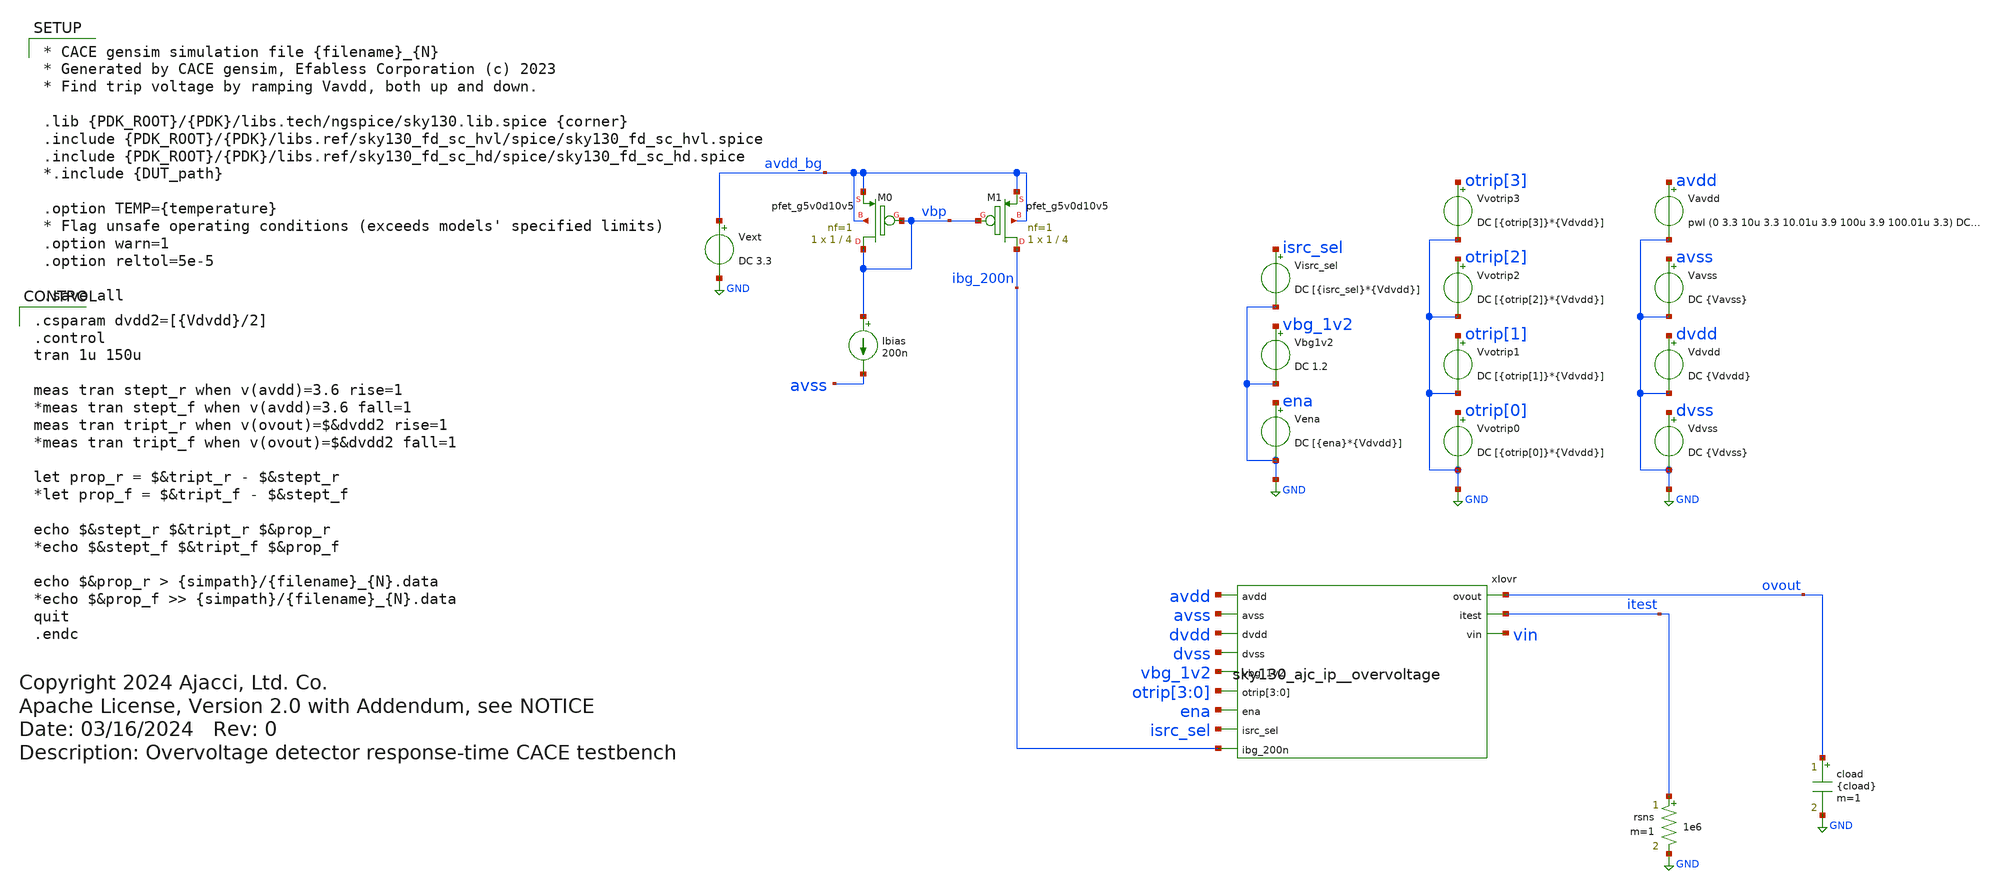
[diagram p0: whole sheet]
** sch_path: cace/response_time.sch
* Copyright 2024 Ajacci, Ltd. Co.
* Apache License, Version 2.0 with Addendum, see NOTICE
**.subckt response_time
Vavss avss GND DC {Vavss}
Vena ena GND DC [{ena}*{Vdvdd}]
Vavdd avdd GND pwl (0 3.3 10u 3.3 10.01u 3.9 100u 3.9 100.01u 3.3) DC {Vavdd}
.save i(vavdd)
Vbg1v2 vbg_1v2 GND DC 1.2
Ibias vbp avss 200n
XM1 ibg_200n vbp avdd_bg avdd_bg sky130_fd_pr__pfet_g5v0d10v5 L=4 W=1 nf=1 ad='int((nf+1)/2) * W/nf * 0.29'
+ as='int((nf+2)/2) * W/nf * 0.29' pd='2*int((nf+1)/2) * (W/nf + 0.29)' ps='2*int((nf+2)/2) * (W/nf + 0.29)'
+ nrd='0.29 / W' nrs='0.29 / W' sa=0 sb=0 sd=0 mult=1 m=1
XM0 vbp vbp avdd_bg avdd_bg sky130_fd_pr__pfet_g5v0d10v5 L=4 W=1 nf=1 ad='int((nf+1)/2) * W/nf * 0.29'
+ as='int((nf+2)/2) * W/nf * 0.29' pd='2*int((nf+1)/2) * (W/nf + 0.29)' ps='2*int((nf+2)/2) * (W/nf + 0.29)'
+ nrd='0.29 / W' nrs='0.29 / W' sa=0 sb=0 sd=0 mult=1 m=1
Vdvss dvss GND DC {Vdvss}
Vdvdd dvdd GND DC {Vdvdd}
.save i(vdvdd)
rsns itest GND 1e6 m=1
cload ovout GND {cload} m=1
xIovr avdd avss dvdd dvss vbg_1v2 ovout itest otrip[3] otrip[2] otrip[1] otrip[0] vin ena isrc_sel
+ ibg_200n sky130_ajc_ip__overvoltage
Vvotrip0 otrip[0] GND DC [{otrip[0]}*{Vdvdd}]
.save i(vvotrip0)
Vvotrip1 otrip[1] GND DC [{otrip[1]}*{Vdvdd}]
.save i(vvotrip1)
Vvotrip2 otrip[2] GND DC [{otrip[2]}*{Vdvdd}]
.save i(vvotrip2)
Vvotrip3 otrip[3] GND DC [{otrip[3]}*{Vdvdd}]
.save i(vvotrip3)
Visrc_sel isrc_sel GND DC [{isrc_sel}*{Vdvdd}]
Vext avdd_bg GND DC 3.3
.save i(vext)
**** begin user architecture code

* CACE gensim simulation file {filename}_{N}
* Generated by CACE gensim, Efabless Corporation (c) 2023
* Find trip voltage by ramping Vavdd, both up and down.

.lib {PDK_ROOT}/{PDK}/libs.tech/ngspice/sky130.lib.spice {corner}
.include {PDK_ROOT}/{PDK}/libs.ref/sky130_fd_sc_hvl/spice/sky130_fd_sc_hvl.spice
.include {PDK_ROOT}/{PDK}/libs.ref/sky130_fd_sc_hd/spice/sky130_fd_sc_hd.spice
*.include {DUT_path}

.option TEMP={temperature}
* Flag unsafe operating conditions (exceeds models' specified limits)
.option warn=1
.option reltol=5e-5

.save all



.csparam dvdd2=[{Vdvdd}/2]
.control
tran 1u 150u

meas tran stept_r when v(avdd)=3.6 rise=1
*meas tran stept_f when v(avdd)=3.6 fall=1
meas tran tript_r when v(ovout)=$&dvdd2 rise=1
*meas tran tript_f when v(ovout)=$&dvdd2 fall=1

let prop_r = $&tript_r - $&stept_r
*let prop_f = $&tript_f - $&stept_f

echo $&stept_r $&tript_r $&prop_r
*echo $&stept_f $&tript_f $&prop_f

echo $&prop_r > {simpath}/{filename}_{N}.data
*echo $&prop_f >> {simpath}/{filename}_{N}.data
quit
.endc


**** end user architecture code
**.ends
.GLOBAL GND
.end
